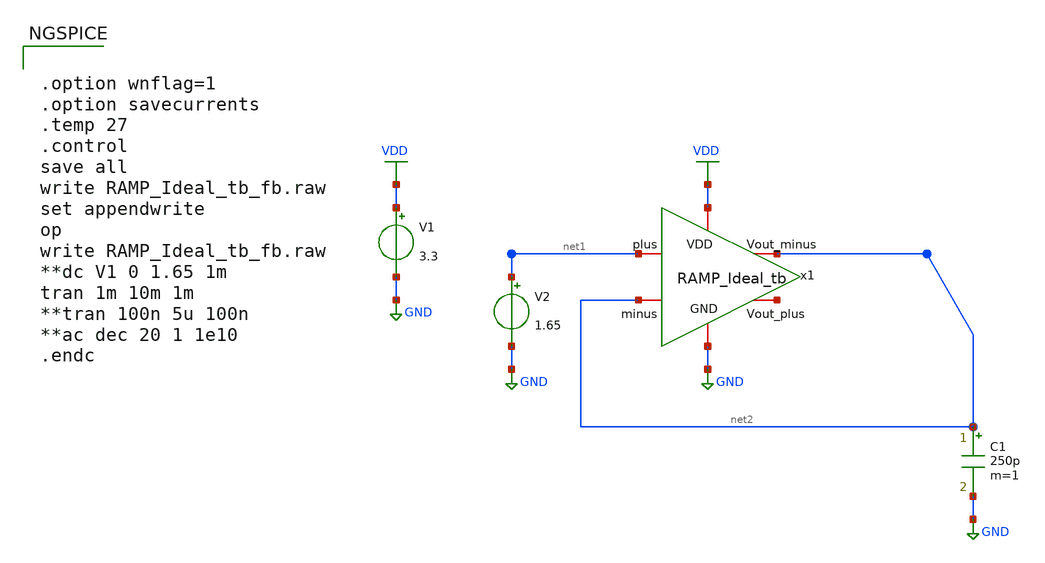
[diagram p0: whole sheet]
** sch_path: Design_Files/RAMP_Ideal/RAMP_Ideal_tb_fb.sch
**.subckt RAMP_Ideal_tb_fb
x1 VDD net1 net2 net3 net2 GND RAMP_Ideal_tb
V1 VDD GND 3.3
V2 net1 GND 1.65
C1 net2 GND 250p m=1
**** begin user architecture code


.option wnflag=1
.option savecurrents
.temp 27
.control
save all
write RAMP_Ideal_tb_fb.raw
set appendwrite
op
write RAMP_Ideal_tb_fb.raw
**dc V1 0 1.65 1m
tran 1m 10m 1m
**tran 100n 5u 100n
**ac dec 20 1 1e10
.endc




.save @m.xm1.m0[gm]
.save @m.xm1.m0[id]
.save @m.xm1.m0[vth]
.save @m.xm1.m0[gds]
.save @m.xm1.m0[cgg]
.save @m.xm1.m0[cgs]
.save @m.xm1.m0[cgd]
.save @m.xm2.m0[gm]
.save @m.xm2.m0[id]
.save @m.xm2.m0[vth]
.save @m.xm2.m0[gds]
.save @m.xm2.m0[cgg]
.save @m.xm2.m0[cgs]
.save @m.xm2.m0[cgd]
.save @m.xm3.m0[gm]
.save @m.xm3.m0[id]
.save @m.xm3.m0[vth]
.save @m.xm3.m0[vds]
.save @m.xm3.m0[gds]
.save @m.xm3.m0[cgg]
.save @m.xm3.m0[cgs]
.save @m.xm3.m0[cgd]
.save @m.xm4.m0[gm]
.save @m.xm4.m0[id]
.save @m.xm4.m0[vth]
.save @m.xm4.m0[vds]
.save @m.xm4.m0[gds]
.save @m.xm4.m0[cgg]
.save @m.xm4.m0[cgs]
.save @m.xm4.m0[cgd]



.lib /foss/pdks/volare/gf180mcu/versions/0fe599b2afb6708d281543108caf8310912f54af/gf180mcuD/libs.tech/ngspice/sm141064.ngspice typical
.include /foss/pdks/volare/gf180mcu/versions/0fe599b2afb6708d281543108caf8310912f54af/gf180mcuD/libs.tech/ngspice/design.ngspice
.lib /foss/pdks/volare/gf180mcu/versions/0fe599b2afb6708d281543108caf8310912f54af/gf180mcuD/libs.tech/ngspice/sm141064.ngspice res_statistical

**.include $::180MCU_MODELS/design.ngspice
**.lib $::180MCU_MODELS/sm141064.ngspice typical
**.lib $::180MCU_MODELS/sm141064.ngspice res_typical
* .lib $::180MCU_MODELS/sm141064.ngspice res_statistical
*.include $::180MCU_MODELS/design.ngspice
*.lib $::180MCU_MODELS/sm141064.ngspice typical


**** end user architecture code
**.ends

* expanding   symbol:  chipathon/RAMP_Ideal/RAMP_Ideal_tb.sym # of pins=6
** sym_path: Design_Files/RAMP_Ideal/RAMP_Ideal_tb.sym
** sch_path: Design_Files/RAMP_Ideal/RAMP_Ideal_tb.sch
.subckt RAMP_Ideal_tb VDD plus Vout_minus Vout_plus minus GND
*.iopin plus
*.iopin minus
*.iopin Vout_minus
*.iopin Vout_plus
*.iopin VDD
*.iopin GND
XM6 Vout_minus net2 VDD VDD pfet_03v3 L=0.5u W=15.375u nf=1 ad='int((nf+1)/2) * W/nf * 0.18u' as='int((nf+2)/2) * W/nf * 0.18u'
+ pd='2*int((nf+1)/2) * (W/nf + 0.18u)' ps='2*int((nf+2)/2) * (W/nf + 0.18u)' nrd='0.18u / W' nrs='0.18u / W'
+ sa=0 sb=0 sd=0 m=8
XM7 Vout_minus net3 GND GND nfet_03v3 L=0.5u W=5u nf=1 ad='int((nf+1)/2) * W/nf * 0.18u' as='int((nf+2)/2) * W/nf * 0.18u'
+ pd='2*int((nf+1)/2) * (W/nf + 0.18u)' ps='2*int((nf+2)/2) * (W/nf + 0.18u)' nrd='0.18u / W' nrs='0.18u / W'
+ sa=0 sb=0 sd=0 m=8
E1 net2 net1 VGP_bias minus 1
E2 net3 net1 VGN_bias minus 1
G1 net1 minus net4 minus 3.99269m
R1 net1 minus 254.648 m=1
C1 net1 minus 50f m=1
R2 net4 minus 254.648 m=1
C2 net4 minus 50f m=1
G2 net4 minus plus minus 7.8539m
XM1 VGN_bias VGN_bias GND GND nfet_03v3 L=0.5u W=5u nf=1 ad='int((nf+1)/2) * W/nf * 0.18u' as='int((nf+2)/2) * W/nf * 0.18u'
+ pd='2*int((nf+1)/2) * (W/nf + 0.18u)' ps='2*int((nf+2)/2) * (W/nf + 0.18u)' nrd='0.18u / W' nrs='0.18u / W'
+ sa=0 sb=0 sd=0 m=8
I0 VDD VGN_bias 10u
XM2 VGP_bias VGP_bias VDD VDD pfet_03v3 L=0.5u W=15.375u nf=1 ad='int((nf+1)/2) * W/nf * 0.18u' as='int((nf+2)/2) * W/nf * 0.18u'
+ pd='2*int((nf+1)/2) * (W/nf + 0.18u)' ps='2*int((nf+2)/2) * (W/nf + 0.18u)' nrd='0.18u / W' nrs='0.18u / W'
+ sa=0 sb=0 sd=0 m=8
I1 VGP_bias GND 10u
XM3 Vout_plus net5 VDD VDD pfet_03v3 L=0.5u W=15.375u nf=1 ad='int((nf+1)/2) * W/nf * 0.18u' as='int((nf+2)/2) * W/nf * 0.18u'
+ pd='2*int((nf+1)/2) * (W/nf + 0.18u)' ps='2*int((nf+2)/2) * (W/nf + 0.18u)' nrd='0.18u / W' nrs='0.18u / W'
+ sa=0 sb=0 sd=0 m=8
XM4 Vout_plus net6 GND GND nfet_03v3 L=0.5u W=5u nf=1 ad='int((nf+1)/2) * W/nf * 0.18u' as='int((nf+2)/2) * W/nf * 0.18u'
+ pd='2*int((nf+1)/2) * (W/nf + 0.18u)' ps='2*int((nf+2)/2) * (W/nf + 0.18u)' nrd='0.18u / W' nrs='0.18u / W'
+ sa=0 sb=0 sd=0 m=8
E3 net5 minus VGP_bias minus 1
E4 net6 minus VGN_bias minus 1
.ends

.GLOBAL GND
.GLOBAL VDD
.end
